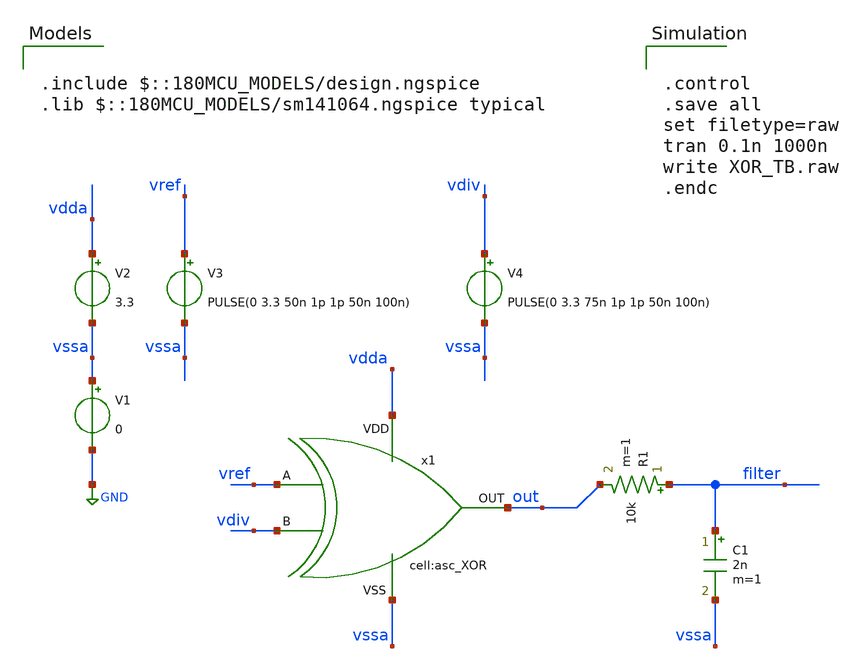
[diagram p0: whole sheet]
** sch_path: designs/libs/tb_analog/tb_asc_PFD_XOR/tb_asc_PFD_XOR.sch
**.subckt tb_asc_PFD_XOR
V1 vssa GND 0
V2 vdda vssa 3.3
V3 vref vssa PULSE(0 3.3 50n 1p 1p 50n 100n)
V4 vdiv vssa PULSE(0 3.3 75n 1p 1p 50n 100n)
x1 vdda vssa out vref vdiv asc_XOR
C1 filter vssa 2n m=1
R1 filter out 10k m=1
**** begin user architecture code

.include $::180MCU_MODELS/design.ngspice
.lib $::180MCU_MODELS/sm141064.ngspice typical



.control
.save all
set filetype=raw
tran 0.1n 1000n
write XOR_TB.raw
.endc


**** end user architecture code
**.ends
.GLOBAL GND
.end
